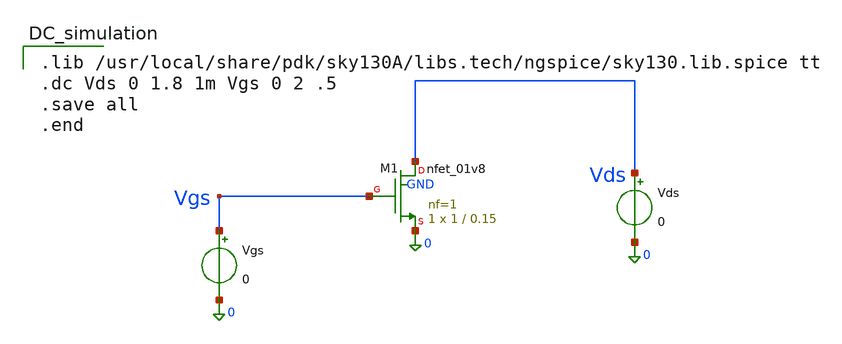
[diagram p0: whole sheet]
** sch_path: nmos_dc_analysis/dc_sweep.sch
**.subckt dc_sweep
XM1 Vds Vgs 0 GND sky130_fd_pr__nfet_01v8 L=0.15 W=1 nf=1 ad='int((1 + 1)/2) * 1 / 1 * 0.29' as='int((1 + 2)/2) * 1 / 1 * 0.29'
+ pd='2*int((1 + 1)/2) * (1 / 1 + 0.29)' ps='2*int((1 + 2)/2) * (1 / 1 + 0.29)' nrd='0.29 / 1 ' nrs='0.29 / 1 '
+ sa=0 sb=0 sd=0 mult=1 m=1
Vgs Vgs 0 0
Vds Vds 0 0
**** begin user architecture code

.lib /usr/local/share/pdk/sky130A/libs.tech/ngspice/sky130.lib.spice tt
.dc Vds 0 1.8 1m Vgs 0 2 .5
.save all
.end

**** end user architecture code
**.ends
.end
